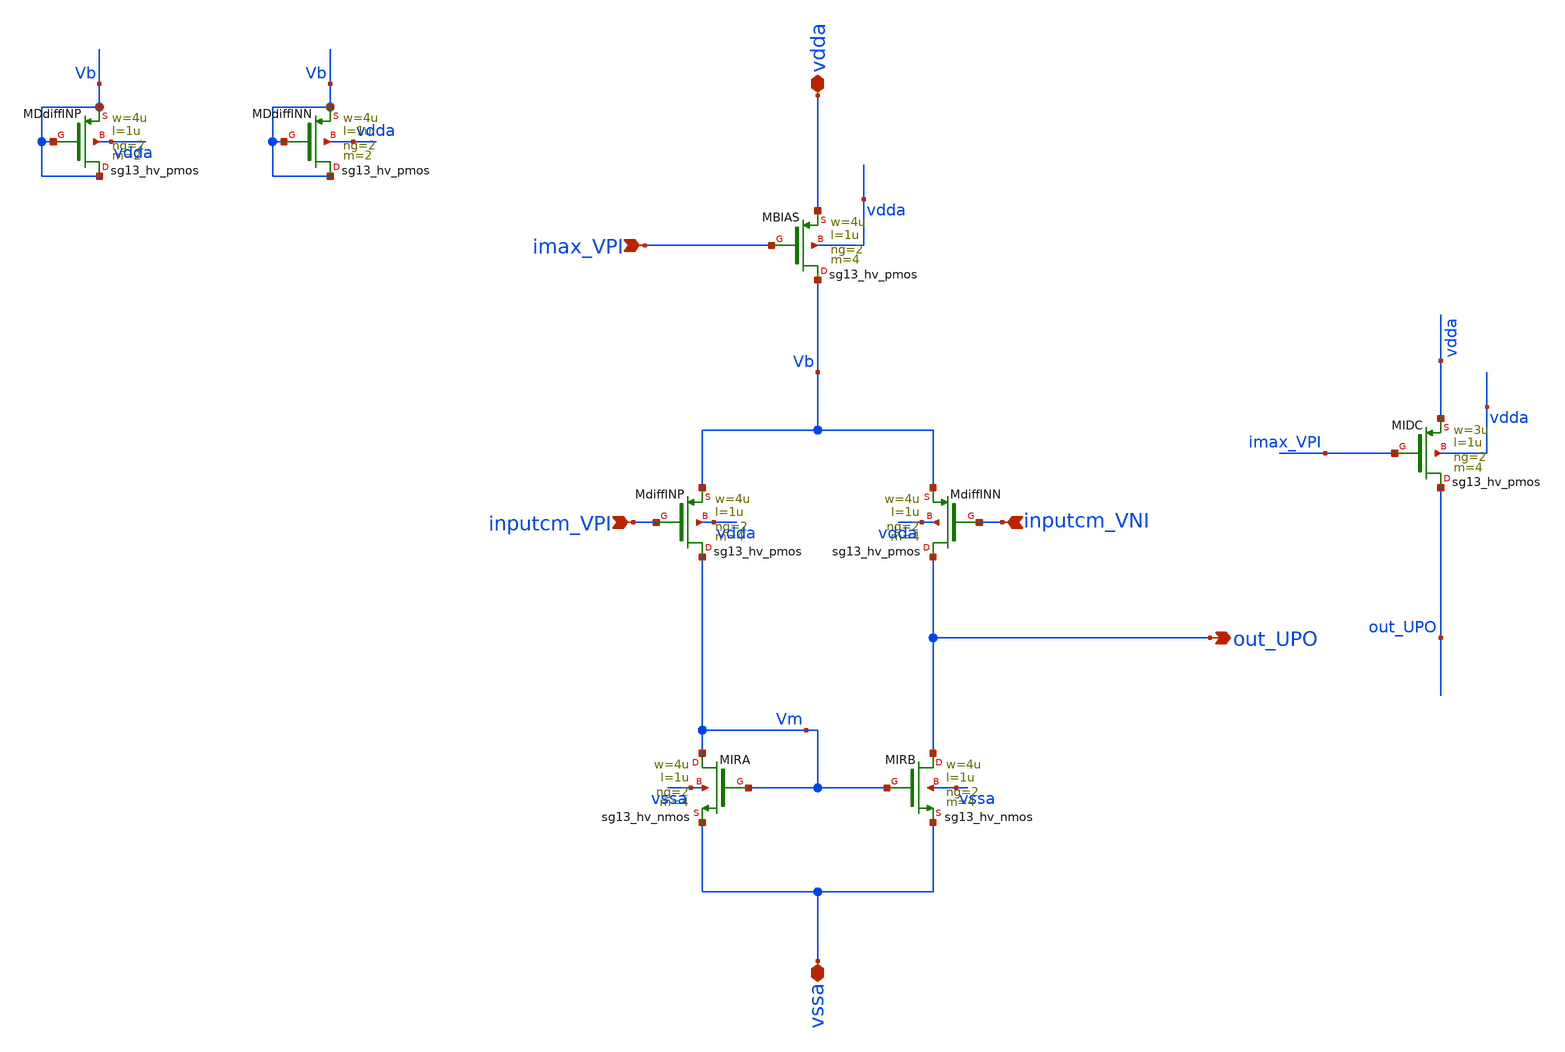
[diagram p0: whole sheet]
** sch_path: V2I.sch
**.subckt V2I inputcm_VNI inputcm_VPI out_UPO imax_VPI vdda vssa
*.ipin inputcm_VNI
*.ipin inputcm_VPI
*.opin out_UPO
*.ipin imax_VPI
*.iopin vdda
*.iopin vssa
XMIRA Vm Vm vssa vssa sg13_hv_nmos w=4u l=1u ng=2 m=4 mm_ok=1
XMBIAS Vb imax_VPI vdda vdda sg13_hv_pmos w=4u l=1u ng=2 m=4 mm_ok=1
XMIRB out_UPO Vm vssa vssa sg13_hv_nmos w=4u l=1u ng=2 m=4 mm_ok=1
XMdiffINN out_UPO inputcm_VNI Vb vdda sg13_hv_pmos w=4u l=1u ng=2 m=4 mm_ok=1
XMIDC out_UPO imax_VPI vdda vdda sg13_hv_pmos w=3u l=1u ng=2 m=4 mm_ok=1
XMdiffINP Vm inputcm_VPI Vb vdda sg13_hv_pmos w=4u l=1u ng=2 m=4 mm_ok=1
XMDdiffINP Vb Vb Vb vdda sg13_hv_pmos w=4u l=1u ng=2 m=2 mm_ok=1
XMDdiffINN Vb Vb Vb vdda sg13_hv_pmos w=4u l=1u ng=2 m=2 mm_ok=1
**.ends
.end
